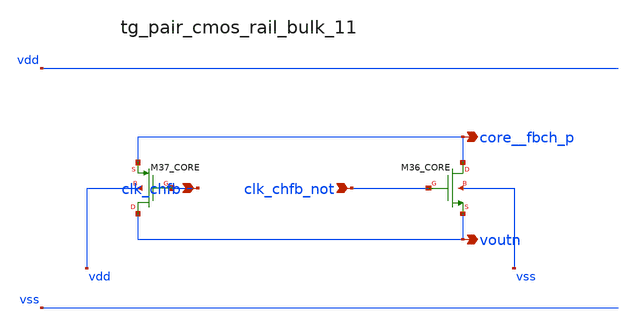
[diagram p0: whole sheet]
** sch_path: analog-db/raw/ia_006_fan_chopper_cmfb/hier/blocks/tg_pair_cmos_rail_bulk_11.sch
**.subckt tg_pair_cmos_rail_bulk_11 clk_chfb clk_chfb_not core__fbch_p voutn
*.ipin clk_chfb
*.ipin clk_chfb_not
*.opin core__fbch_p
*.opin voutn
XM36_CORE core__fbch_p clk_chfb_not voutn vss sg13_lv_nmos w=x_dut_xm36_core_w l=x_dut_xm36_core_l
+ ng=1 m=x_dut_xm36_core_m
XM37_CORE voutn clk_chfb core__fbch_p vdd sg13_lv_pmos w=x_dut_xm37_core_w l=x_dut_xm37_core_l ng=1
+ m=x_dut_xm37_core_m
**.ends
.end
